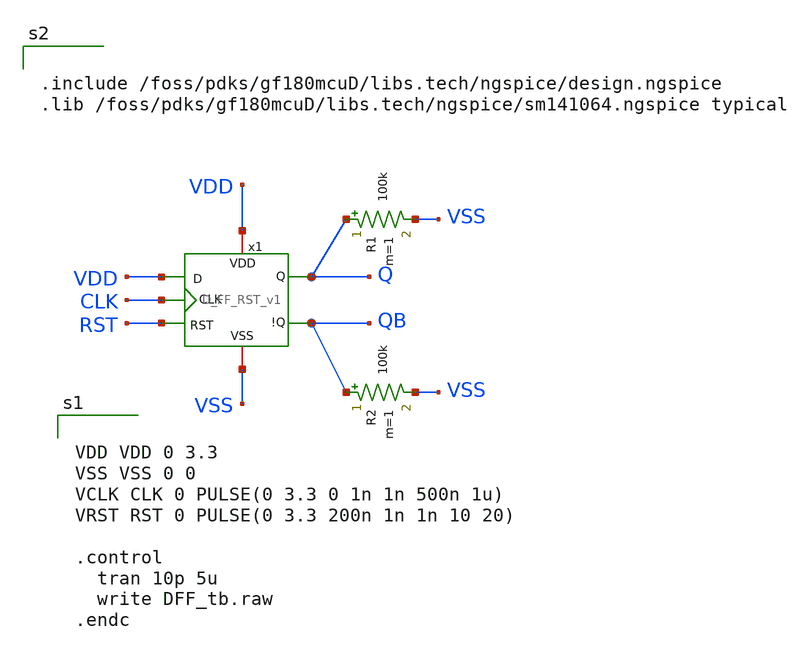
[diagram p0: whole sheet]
** sch_path: team_src/xschem/D_FF_RST_v1_tb.sch
**.subckt D_FF_RST_v1_tb
x1 RST VDD VDD Q CLK QB VSS D_FF_RST_v1
R1 Q VSS 100k m=1
R2 QB VSS 100k m=1
**** begin user architecture code


VDD VDD 0 3.3
VSS VSS 0 0
VCLK CLK 0 PULSE(0 3.3 0 1n 1n 500n 1u)
VRST RST 0 PULSE(0 3.3 200n 1n 1n 10 20)

.control
  tran 10p 5u
  write DFF_tb.raw
.endc




.include /foss/pdks/gf180mcuD/libs.tech/ngspice/design.ngspice
.lib /foss/pdks/gf180mcuD/libs.tech/ngspice/sm141064.ngspice typical


**** end user architecture code
**.ends

* expanding   symbol:  D_FF_RST_v1.sym # of pins=7
** sym_path: team_src/xschem/D_FF_RST_v1.sym
** sch_path: team_src/xschem/D_FF_RST_v1.sch
.subckt D_FF_RST_v1 RST VDD D Q CLK !Q VSS
*.ipin CLK
*.ipin D
*.iopin VDD
*.opin Q
*.opin !Q
*.iopin VSS
*.ipin RST
x1 VDD Q net5 !Q VSS NAND_v1
x3 VDD net7 D net2 VSS NAND_v1
x4 VDD net6 net1 net2 VSS NAND_v1
x5 VDD D net1 VSS NOT_v1
x6 VDD net3 net2 VSS NOT_v1
x7 VDD CLK net4 VSS NOT_v1
x8 VDD net3 CLK net4 VSS NAND_v1
x2 RST VDD !Q Q net6 VSS NAND3_v1
x9 VDD net7 net8 VSS NOT_v1
x10 VDD net5 net8 RST VSS NAND_v1
.ends


* expanding   symbol:  NAND_v1.sym # of pins=5
** sym_path: team_src/xschem/NAND_v1.sym
** sch_path: team_src/xschem/NAND_v1.sch
.subckt NAND_v1 VDD Y A B VSS
*.iopin VSS
*.iopin VDD
*.ipin A
*.opin Y
*.ipin B
XM1 net1 B VSS VSS nfet_03v3 L=0.28u W=1u nf=1 ad='int((nf+1)/2) * W/nf * 0.18u' as='int((nf+2)/2) * W/nf * 0.18u'
+ pd='2*int((nf+1)/2) * (W/nf + 0.18u)' ps='2*int((nf+2)/2) * (W/nf + 0.18u)' nrd='0.18u / W' nrs='0.18u / W'
+ sa=0 sb=0 sd=0 m=1
XM2 Y A net1 VSS nfet_03v3 L=0.28u W=1u nf=1 ad='int((nf+1)/2) * W/nf * 0.18u' as='int((nf+2)/2) * W/nf * 0.18u'
+ pd='2*int((nf+1)/2) * (W/nf + 0.18u)' ps='2*int((nf+2)/2) * (W/nf + 0.18u)' nrd='0.18u / W' nrs='0.18u / W'
+ sa=0 sb=0 sd=0 m=1
XM3 Y B VDD VDD pfet_03v3 L=0.28u W=1u nf=1 ad='int((nf+1)/2) * W/nf * 0.18u' as='int((nf+2)/2) * W/nf * 0.18u'
+ pd='2*int((nf+1)/2) * (W/nf + 0.18u)' ps='2*int((nf+2)/2) * (W/nf + 0.18u)' nrd='0.18u / W' nrs='0.18u / W'
+ sa=0 sb=0 sd=0 m=1
XM4 Y A VDD VDD pfet_03v3 L=0.28u W=1u nf=1 ad='int((nf+1)/2) * W/nf * 0.18u' as='int((nf+2)/2) * W/nf * 0.18u'
+ pd='2*int((nf+1)/2) * (W/nf + 0.18u)' ps='2*int((nf+2)/2) * (W/nf + 0.18u)' nrd='0.18u / W' nrs='0.18u / W'
+ sa=0 sb=0 sd=0 m=1
.ends


* expanding   symbol:  NOT_v1.sym # of pins=4
** sym_path: team_src/xschem/NOT_v1.sym
** sch_path: team_src/xschem/NOT_v1.sch
.subckt NOT_v1 VDD A Y VSS
*.iopin VSS
*.iopin VDD
*.ipin A
*.opin Y
XM2 Y A VSS VSS nfet_03v3 L=0.28u W=1u nf=1 ad='int((nf+1)/2) * W/nf * 0.18u' as='int((nf+2)/2) * W/nf * 0.18u'
+ pd='2*int((nf+1)/2) * (W/nf + 0.18u)' ps='2*int((nf+2)/2) * (W/nf + 0.18u)' nrd='0.18u / W' nrs='0.18u / W'
+ sa=0 sb=0 sd=0 m=1
XM4 Y A VDD VDD pfet_03v3 L=0.28u W=1u nf=1 ad='int((nf+1)/2) * W/nf * 0.18u' as='int((nf+2)/2) * W/nf * 0.18u'
+ pd='2*int((nf+1)/2) * (W/nf + 0.18u)' ps='2*int((nf+2)/2) * (W/nf + 0.18u)' nrd='0.18u / W' nrs='0.18u / W'
+ sa=0 sb=0 sd=0 m=1
.ends


* expanding   symbol:  NAND3_v1.sym # of pins=6
** sym_path: team_src/xschem/NAND3_v1.sym
** sch_path: team_src/xschem/NAND3_v1.sch
.subckt NAND3_v1 C VDD Y A B VSS
*.iopin VSS
*.iopin VDD
*.ipin A
*.opin Y
*.ipin B
*.ipin C
XM1 net1 B net2 VSS nfet_03v3 L=0.28u W=3u nf=1 ad='int((nf+1)/2) * W/nf * 0.18u' as='int((nf+2)/2) * W/nf * 0.18u'
+ pd='2*int((nf+1)/2) * (W/nf + 0.18u)' ps='2*int((nf+2)/2) * (W/nf + 0.18u)' nrd='0.18u / W' nrs='0.18u / W'
+ sa=0 sb=0 sd=0 m=1
XM2 Y A net1 VSS nfet_03v3 L=0.28u W=3u nf=1 ad='int((nf+1)/2) * W/nf * 0.18u' as='int((nf+2)/2) * W/nf * 0.18u'
+ pd='2*int((nf+1)/2) * (W/nf + 0.18u)' ps='2*int((nf+2)/2) * (W/nf + 0.18u)' nrd='0.18u / W' nrs='0.18u / W'
+ sa=0 sb=0 sd=0 m=1
XM3 Y B VDD VDD pfet_03v3 L=0.28u W=1u nf=1 ad='int((nf+1)/2) * W/nf * 0.18u' as='int((nf+2)/2) * W/nf * 0.18u'
+ pd='2*int((nf+1)/2) * (W/nf + 0.18u)' ps='2*int((nf+2)/2) * (W/nf + 0.18u)' nrd='0.18u / W' nrs='0.18u / W'
+ sa=0 sb=0 sd=0 m=1
XM4 Y A VDD VDD pfet_03v3 L=0.28u W=1u nf=1 ad='int((nf+1)/2) * W/nf * 0.18u' as='int((nf+2)/2) * W/nf * 0.18u'
+ pd='2*int((nf+1)/2) * (W/nf + 0.18u)' ps='2*int((nf+2)/2) * (W/nf + 0.18u)' nrd='0.18u / W' nrs='0.18u / W'
+ sa=0 sb=0 sd=0 m=1
XM5 Y C VDD VDD pfet_03v3 L=0.28u W=1u nf=1 ad='int((nf+1)/2) * W/nf * 0.18u' as='int((nf+2)/2) * W/nf * 0.18u'
+ pd='2*int((nf+1)/2) * (W/nf + 0.18u)' ps='2*int((nf+2)/2) * (W/nf + 0.18u)' nrd='0.18u / W' nrs='0.18u / W'
+ sa=0 sb=0 sd=0 m=1
XM6 net2 C VSS VSS nfet_03v3 L=0.28u W=3u nf=1 ad='int((nf+1)/2) * W/nf * 0.18u' as='int((nf+2)/2) * W/nf * 0.18u'
+ pd='2*int((nf+1)/2) * (W/nf + 0.18u)' ps='2*int((nf+2)/2) * (W/nf + 0.18u)' nrd='0.18u / W' nrs='0.18u / W'
+ sa=0 sb=0 sd=0 m=1
.ends

.end
